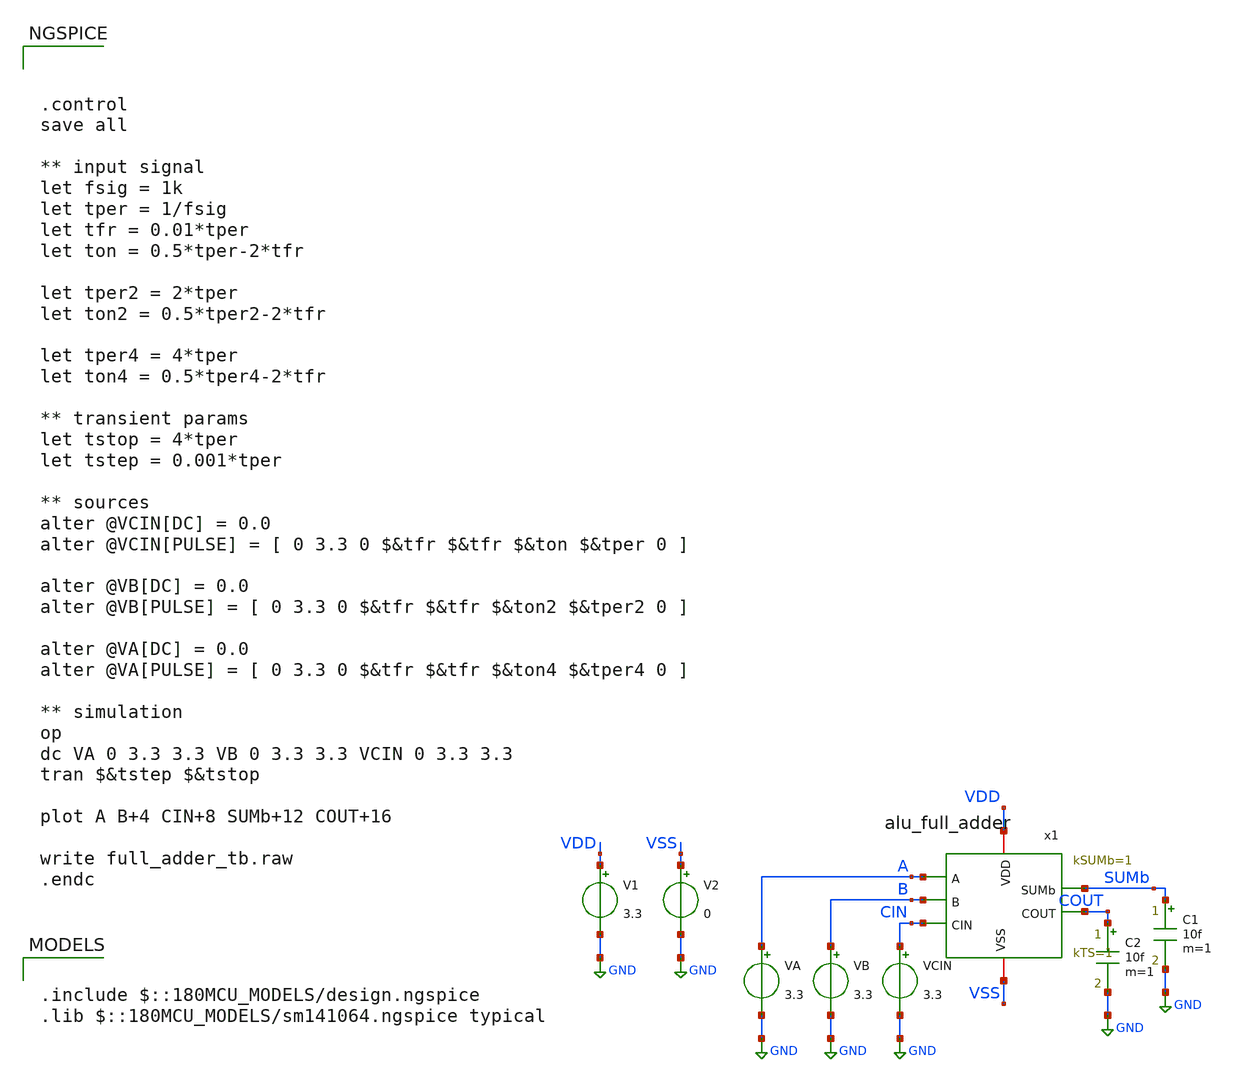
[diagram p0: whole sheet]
** sch_path: CAD4/full_adder_tb.sch
**.subckt full_adder_tb
V1 VDD GND 3.3
VA A GND 3.3
VB B GND 3.3
VCIN CIN GND 3.3
C1 SUMb GND 10f m=1
V2 VSS GND 0
x1 VDD VSS A B CIN SUMb COUT alu_full_adder kSUMb=1 kTS=1
C2 COUT GND 10f m=1
**** begin user architecture code

.include $::180MCU_MODELS/design.ngspice
.lib $::180MCU_MODELS/sm141064.ngspice typical




.control
save all

** input signal
let fsig = 1k
let tper = 1/fsig
let tfr = 0.01*tper
let ton = 0.5*tper-2*tfr

let tper2 = 2*tper
let ton2 = 0.5*tper2-2*tfr

let tper4 = 4*tper
let ton4 = 0.5*tper4-2*tfr

** transient params
let tstop = 4*tper
let tstep = 0.001*tper

** sources
alter @VCIN[DC] = 0.0
alter @VCIN[PULSE] = [ 0 3.3 0 $&tfr $&tfr $&ton $&tper 0 ]

alter @VB[DC] = 0.0
alter @VB[PULSE] = [ 0 3.3 0 $&tfr $&tfr $&ton2 $&tper2 0 ]

alter @VA[DC] = 0.0
alter @VA[PULSE] = [ 0 3.3 0 $&tfr $&tfr $&ton4 $&tper4 0 ]

** simulation
op
dc VA 0 3.3 3.3 VB 0 3.3 3.3 VCIN 0 3.3 3.3
tran $&tstep $&tstop

plot A B+4 CIN+8 SUMb+12 COUT+16

write full_adder_tb.raw
.endc


**** end user architecture code
**.ends
.GLOBAL GND
.end
